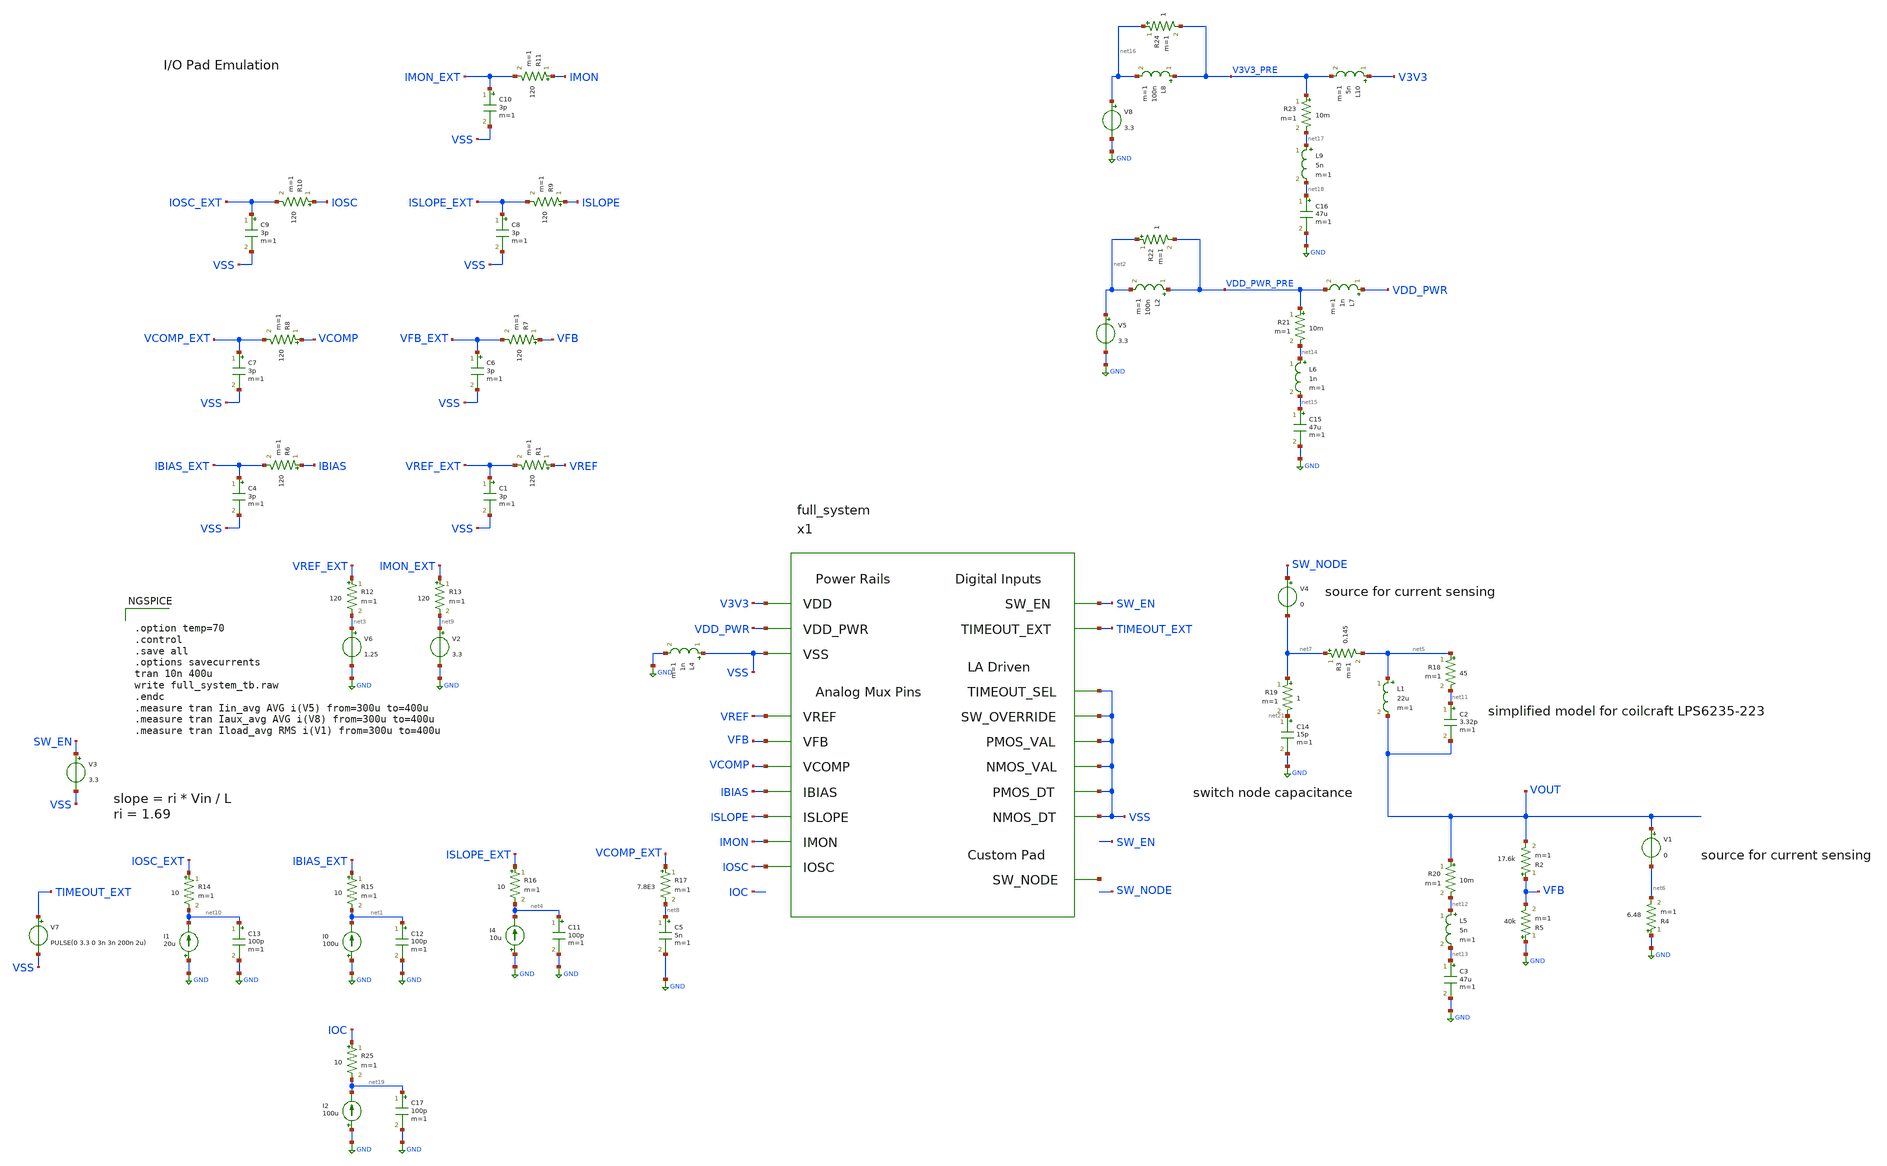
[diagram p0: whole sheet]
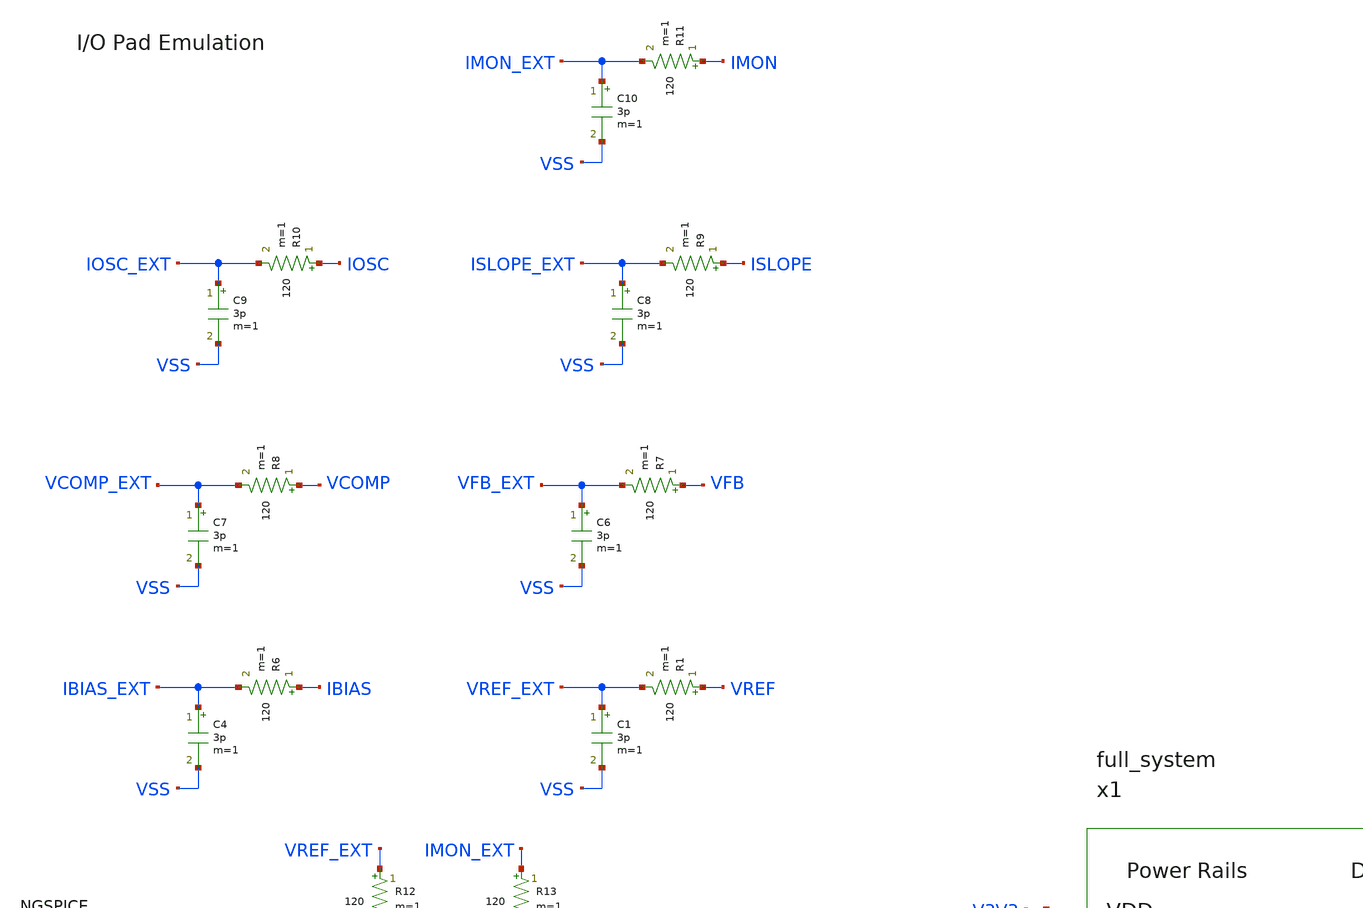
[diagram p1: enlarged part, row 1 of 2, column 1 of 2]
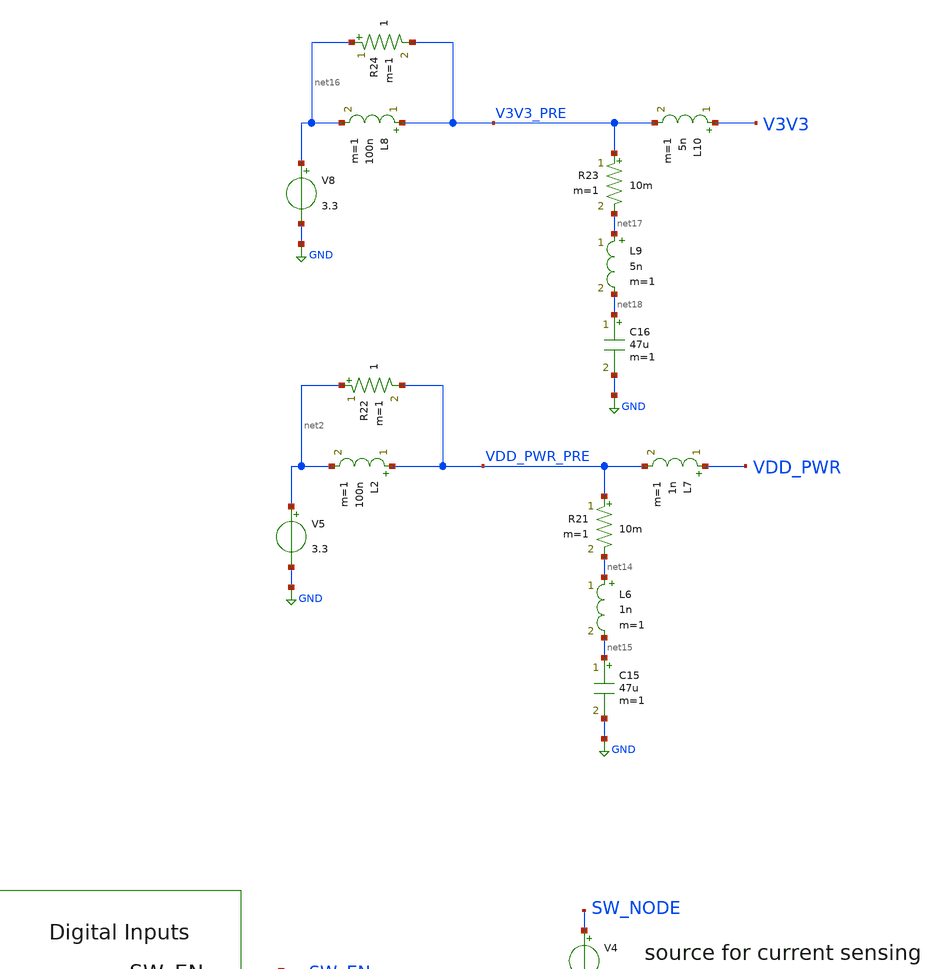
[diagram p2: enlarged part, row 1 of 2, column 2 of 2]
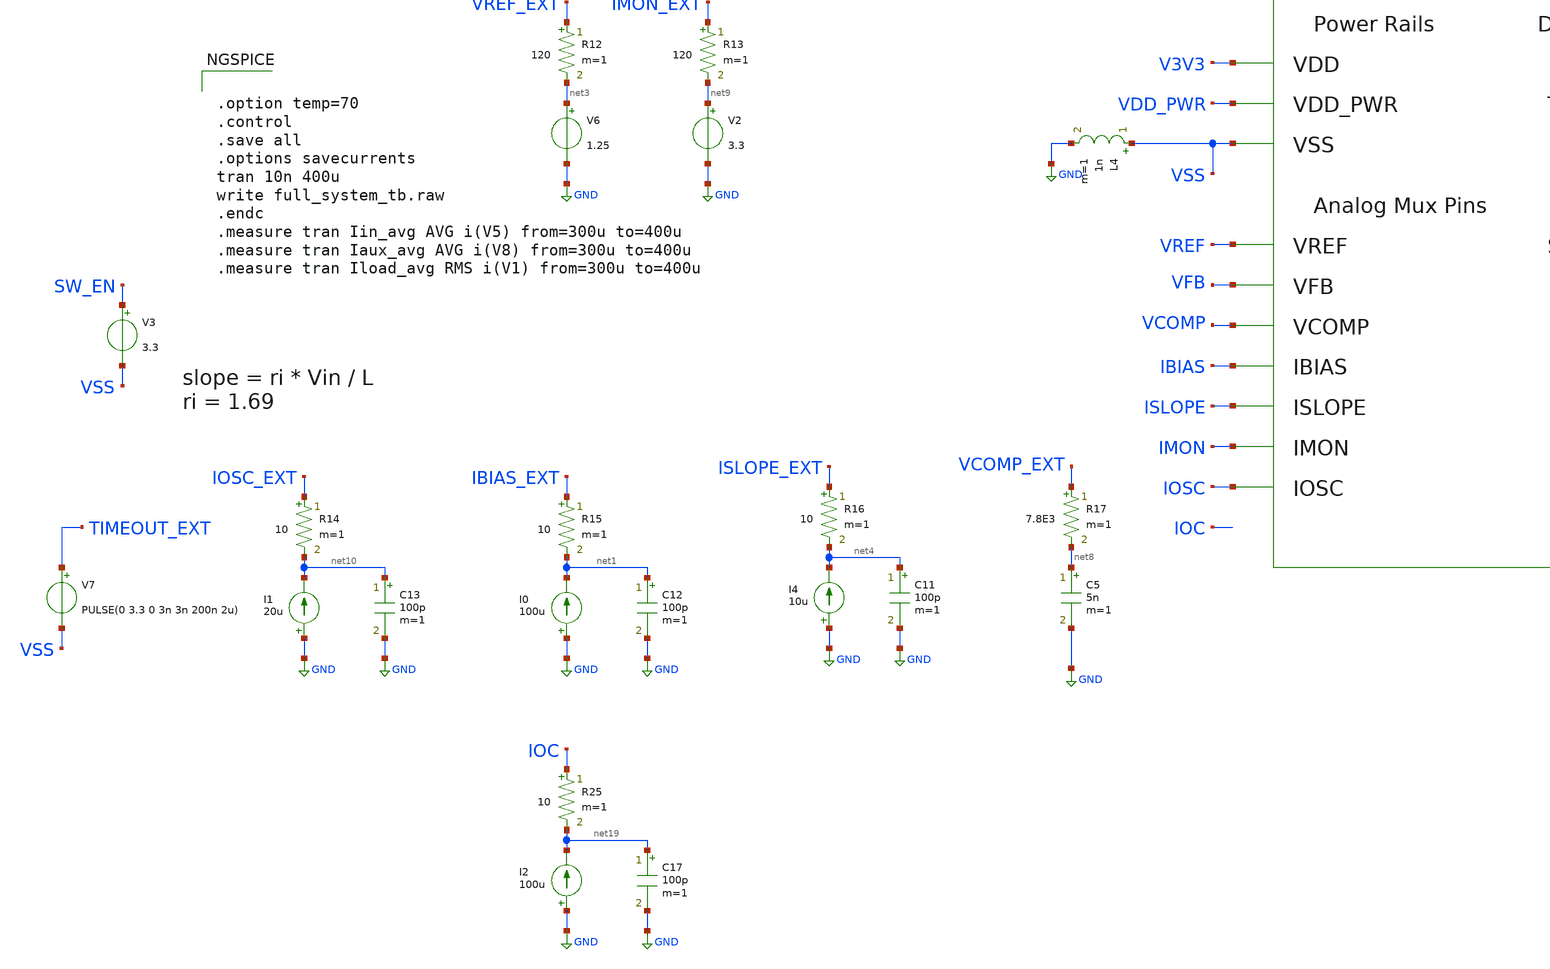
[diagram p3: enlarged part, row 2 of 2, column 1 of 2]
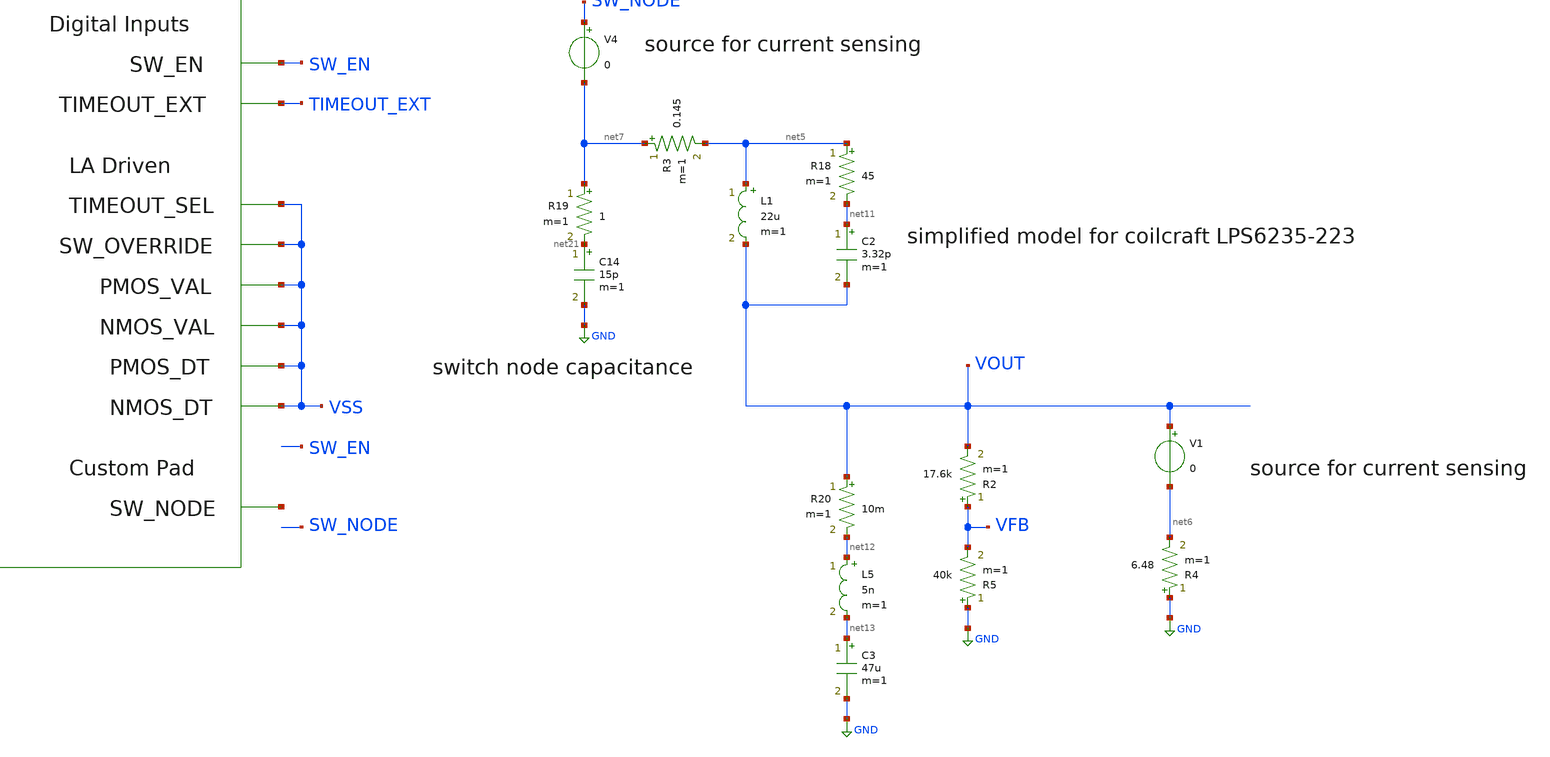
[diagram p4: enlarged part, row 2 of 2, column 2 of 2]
** sch_path: design/system/full_system_tb.sch
**.subckt full_system_tb
I0 GND net1 100u
V5 net2 GND 3.3
V6 net3 GND 1.25
I4 GND net4 10u
x1 V3V3 VDD_PWR VSS VREF VFB VCOMP IBIAS ISLOPE IMON IOSC SW_EN TIMEOUT_EXT VSS VSS VSS VSS VSS VSS
+ net20 full_system
L1 net5 VOUT 22u m=1
R3 net7 net5 0.145 m=1
C2 net11 VOUT 3.32p m=1
C3 net13 GND 47u m=1
R4 GND net6 6.48 m=1
V4 SW_NODE net7 0
R2 VFB VOUT 17.6k m=1
R5 GND VFB 40k m=1
C5 net8 GND 5n m=1
V2 net9 GND 3.3
I1 GND net10 20u
V7 TIMEOUT_EXT VSS PULSE(0 3.3 0 3n 3n 200n 2u)
V3 SW_EN VSS 3.3
R1 VREF VREF_EXT 120 m=1
C1 VREF_EXT VSS 3p m=1
R6 IBIAS IBIAS_EXT 120 m=1
C4 IBIAS_EXT VSS 3p m=1
R7 VFB VFB_EXT 120 m=1
C6 VFB_EXT VSS 3p m=1
R8 VCOMP VCOMP_EXT 120 m=1
C7 VCOMP_EXT VSS 3p m=1
R9 ISLOPE ISLOPE_EXT 120 m=1
C8 ISLOPE_EXT VSS 3p m=1
R10 IOSC IOSC_EXT 120 m=1
C9 IOSC_EXT VSS 3p m=1
R11 IMON IMON_EXT 120 m=1
C10 IMON_EXT VSS 3p m=1
R12 VREF_EXT net3 120 m=1
R13 IMON_EXT net9 120 m=1
R14 IOSC_EXT net10 10 m=1
R15 IBIAS_EXT net1 10 m=1
R16 ISLOPE_EXT net4 10 m=1
R17 VCOMP_EXT net8 7.8E3 m=1
L2 VDD_PWR_PRE net2 100n m=1
L4 VSS GND 1n m=1
C11 net4 GND 100p m=1
C12 net1 GND 100p m=1
C13 net10 GND 100p m=1
R18 net5 net11 45 m=1
C14 net21 GND 15p m=1
R19 net7 net21 1 m=1
L5 net12 net13 5n m=1
R20 VOUT net12 10m m=1
C15 net15 GND 47u m=1
L6 net14 net15 1n m=1
R21 VDD_PWR_PRE net14 10m m=1
L7 VDD_PWR VDD_PWR_PRE 1n m=1
R22 net2 VDD_PWR_PRE 1 m=1
V8 net16 GND 3.3
L8 V3V3_PRE net16 100n m=1
C16 net18 GND 47u m=1
L9 net17 net18 5n m=1
R23 V3V3_PRE net17 10m m=1
L10 V3V3 V3V3_PRE 5n m=1
R24 net16 V3V3_PRE 1 m=1
V1 VOUT net6 0
I2 GND net19 100u
R25 IOC net19 10 m=1
C17 net19 GND 100p m=1
**** begin user architecture code


.option temp=70
.control
.save all
.options savecurrents
tran 10n 400u
write full_system_tb.raw
.endc
.measure tran Iin_avg AVG i(V5) from=300u to=400u
.measure tran Iaux_avg AVG i(V8) from=300u to=400u
.measure tran Iload_avg RMS i(V1) from=300u to=400u



.lib $::SKYWATER_MODELS/models/sky130.lib.spice ss
.option wnflag=1

**** end user architecture code
**.ends
.GLOBAL GND
**** begin user architecture code
[sky130_models]
**** end user architecture code
.end
